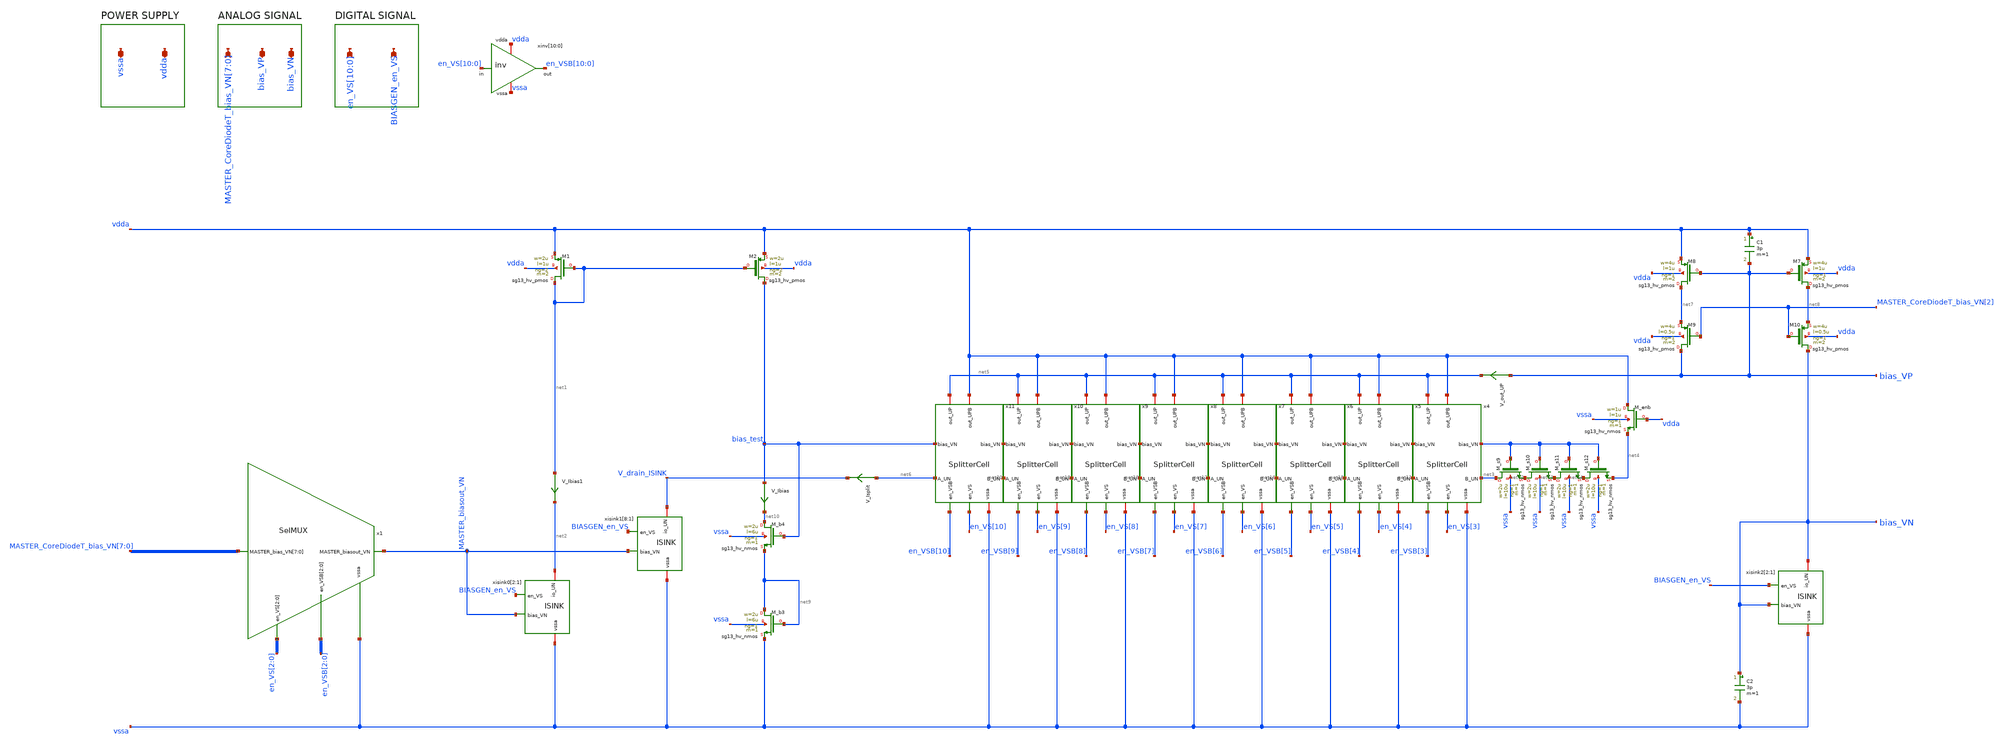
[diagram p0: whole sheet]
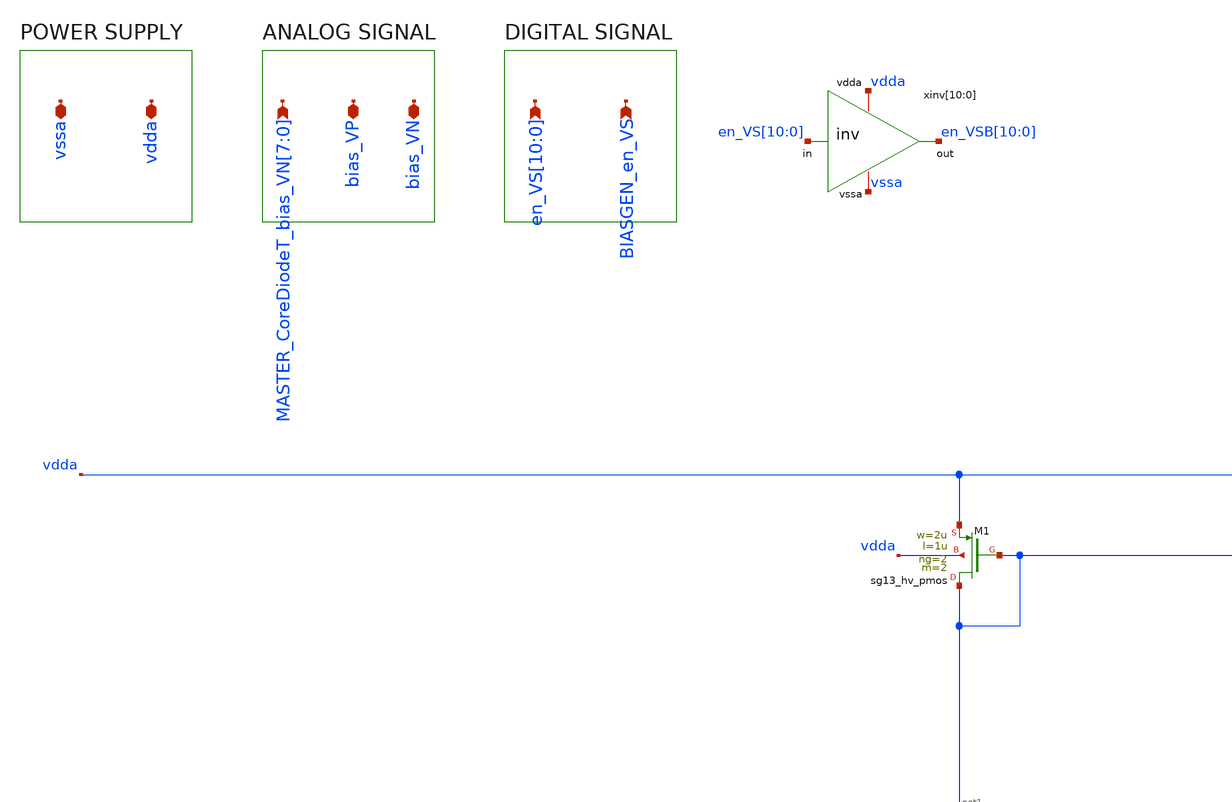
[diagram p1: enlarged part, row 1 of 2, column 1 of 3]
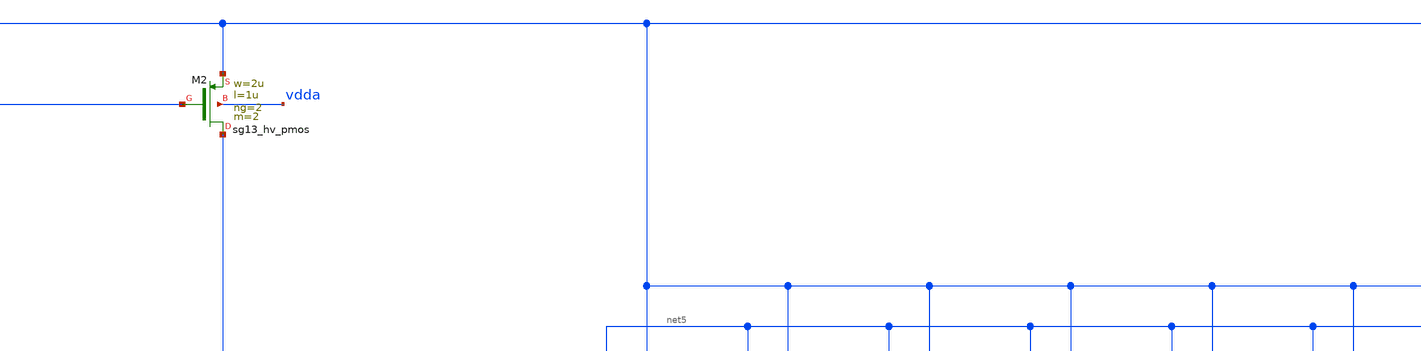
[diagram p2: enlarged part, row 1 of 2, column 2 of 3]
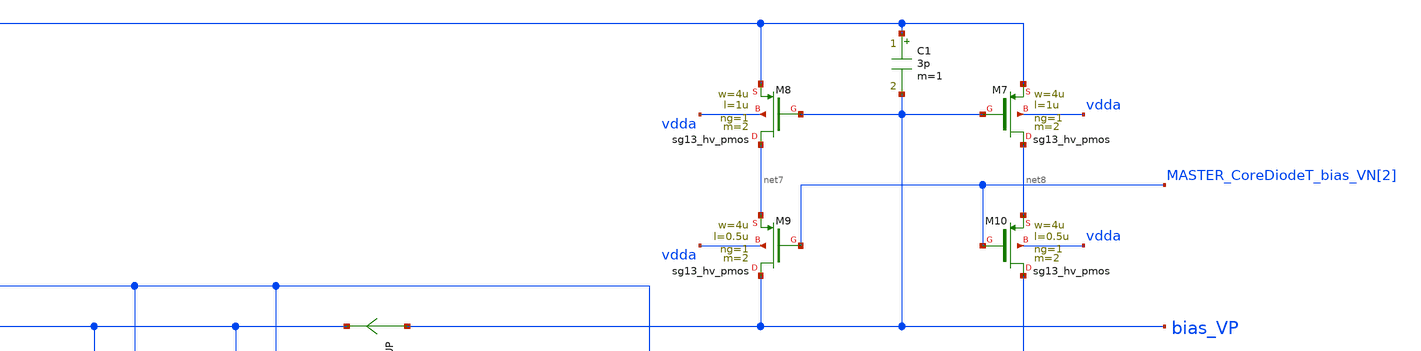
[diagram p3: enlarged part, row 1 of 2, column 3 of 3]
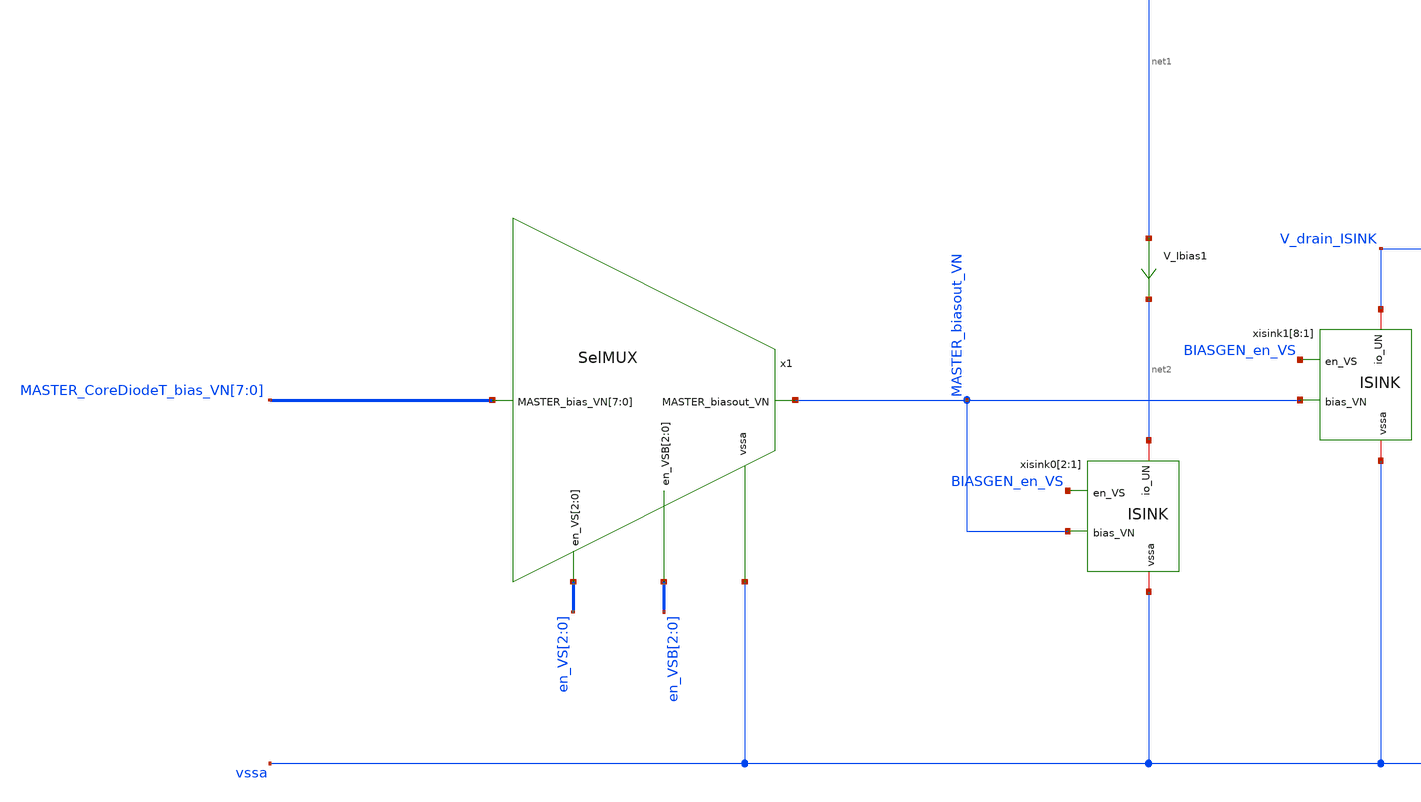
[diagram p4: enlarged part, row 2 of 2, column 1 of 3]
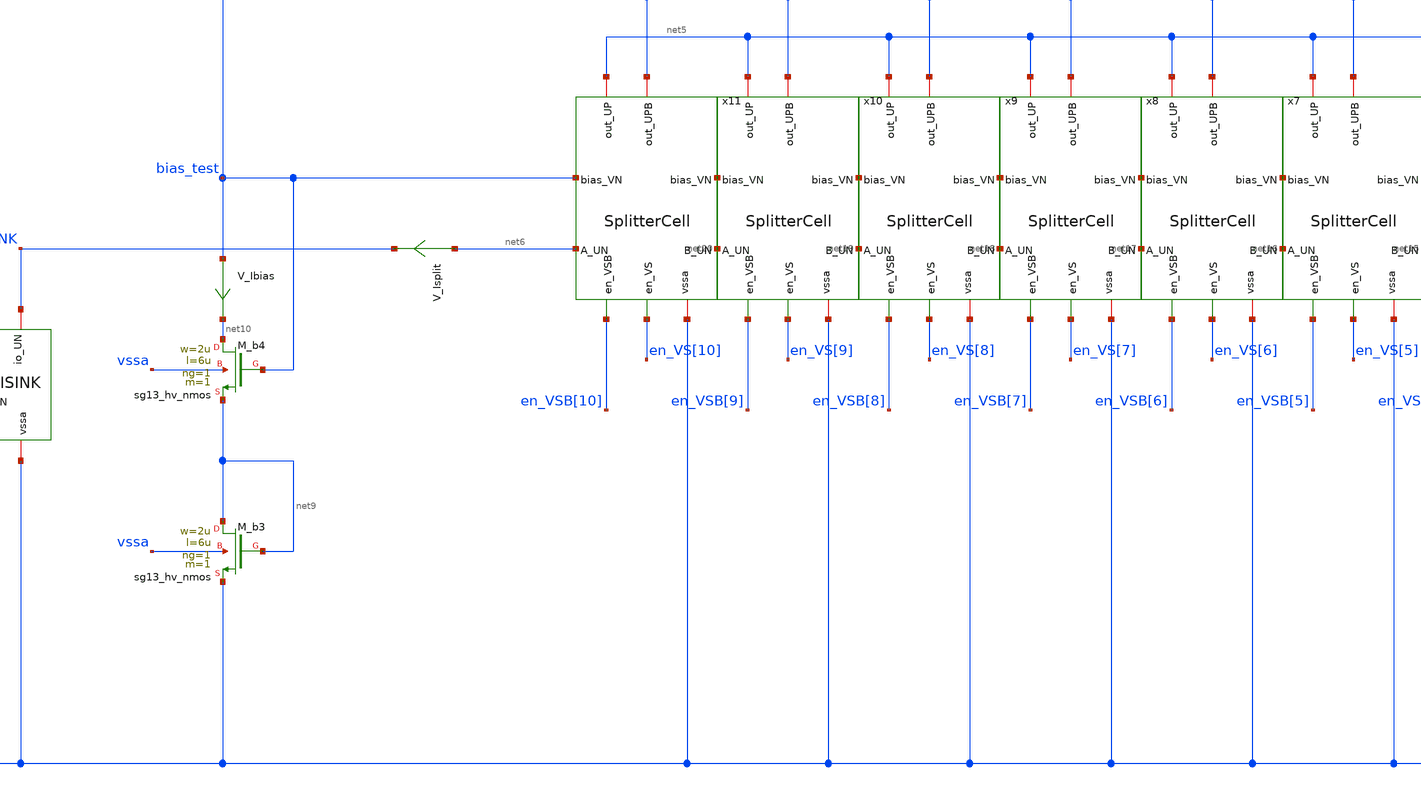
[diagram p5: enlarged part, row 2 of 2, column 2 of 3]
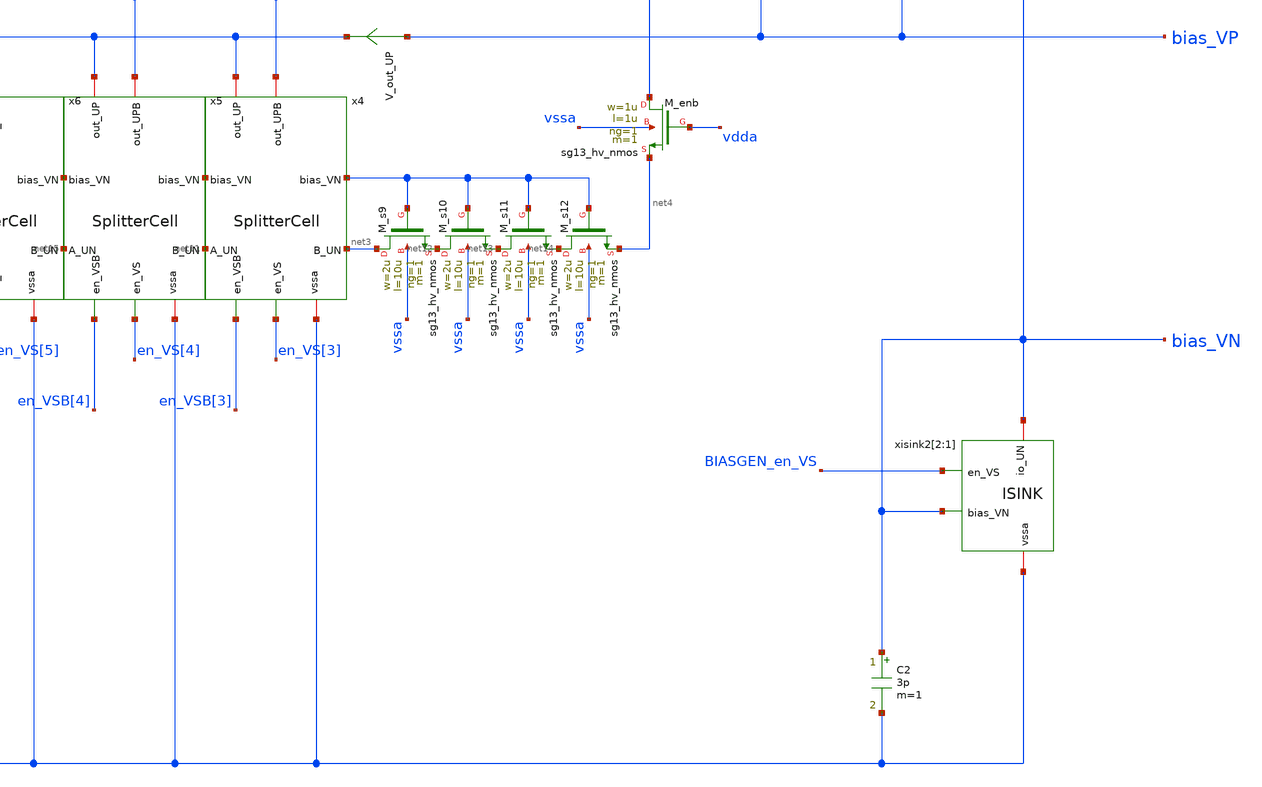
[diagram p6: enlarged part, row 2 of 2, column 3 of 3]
** sch_path: CoreFineDAC_N.sch
**.subckt CoreFineDAC_N
*+ MASTER_CoreDiodeT_bias_VN[7],MASTER_CoreDiodeT_bias_VN[6],MASTER_CoreDiodeT_bias_VN[5],MASTER_CoreDiodeT_bias_VN[4],MASTER_CoreDiodeT_bias_VN[3],MASTER_CoreDiodeT_bias_VN[2],MASTER_CoreDiodeT_bias_VN[1],MASTER_CoreDiodeT_bias_VN[0] en_VS[10],en_VS[9],en_VS[8],en_VS[7],en_VS[6],en_VS[5],en_VS[4],en_VS[3],en_VS[2],en_VS[1],en_VS[0]
*+ vssa vdda bias_VP bias_VN BIASGEN_en_VS
*.ipin
*+ MASTER_CoreDiodeT_bias_VN[7],MASTER_CoreDiodeT_bias_VN[6],MASTER_CoreDiodeT_bias_VN[5],MASTER_CoreDiodeT_bias_VN[4],MASTER_CoreDiodeT_bias_VN[3],MASTER_CoreDiodeT_bias_VN[2],MASTER_CoreDiodeT_bias_VN[1],MASTER_CoreDiodeT_bias_VN[0]
*.ipin
*+ en_VS[10],en_VS[9],en_VS[8],en_VS[7],en_VS[6],en_VS[5],en_VS[4],en_VS[3],en_VS[2],en_VS[1],en_VS[0]
*.iopin vssa
*.iopin vdda
*.iopin bias_VP
*.iopin bias_VN
*.ipin BIASGEN_en_VS
xinv[10] vdda en_VSB[10] en_VS[10] vssa inv
xinv[9] vdda en_VSB[9] en_VS[9] vssa inv
xinv[8] vdda en_VSB[8] en_VS[8] vssa inv
xinv[7] vdda en_VSB[7] en_VS[7] vssa inv
xinv[6] vdda en_VSB[6] en_VS[6] vssa inv
xinv[5] vdda en_VSB[5] en_VS[5] vssa inv
xinv[4] vdda en_VSB[4] en_VS[4] vssa inv
xinv[3] vdda en_VSB[3] en_VS[3] vssa inv
xinv[2] vdda en_VSB[2] en_VS[2] vssa inv
xinv[1] vdda en_VSB[1] en_VS[1] vssa inv
xinv[0] vdda en_VSB[0] en_VS[0] vssa inv
x1 MASTER_CoreDiodeT_bias_VN[7] MASTER_CoreDiodeT_bias_VN[6] MASTER_CoreDiodeT_bias_VN[5]
+ MASTER_CoreDiodeT_bias_VN[4] MASTER_CoreDiodeT_bias_VN[3] MASTER_CoreDiodeT_bias_VN[2] MASTER_CoreDiodeT_bias_VN[1]
+ MASTER_CoreDiodeT_bias_VN[0] vssa en_VS[2] en_VS[1] en_VS[0] en_VSB[2] en_VSB[1] en_VSB[0] MASTER_biasout_VN SelMUX
xisink0[2] MASTER_biasout_VN vssa BIASGEN_en_VS net2 ISINK
xisink0[1] MASTER_biasout_VN vssa BIASGEN_en_VS net2 ISINK
XM1 net1 net1 vdda vdda sg13_hv_pmos w=2u l=1u ng=2 m=2 mm_ok=1
XM2 bias_test net1 vdda vdda sg13_hv_pmos w=2u l=1u ng=2 m=2 mm_ok=1
x4 en_VS[3] net11 net3 en_VSB[3] bias_test vssa vdda net5 SplitterCell
XM_enb vdda vdda net4 vssa sg13_hv_nmos w=1u l=1u ng=1 m=1 mm_ok=1
XM_s9 net3 bias_test net12 vssa sg13_hv_nmos w=2u l=10u ng=1 m=1 mm_ok=1
XM_s10 net12 bias_test net13 vssa sg13_hv_nmos w=2u l=10u ng=1 m=1 mm_ok=1
XM_s11 net13 bias_test net14 vssa sg13_hv_nmos w=2u l=10u ng=1 m=1 mm_ok=1
XM_s12 net14 bias_test net4 vssa sg13_hv_nmos w=2u l=10u ng=1 m=1 mm_ok=1
V_out_UP bias_VP net5 0
.save i(v_out_up)
x5 en_VS[4] net15 net11 en_VSB[4] bias_test vssa vdda net5 SplitterCell
x6 en_VS[5] net16 net15 en_VSB[5] bias_test vssa vdda net5 SplitterCell
x7 en_VS[6] net17 net16 en_VSB[6] bias_test vssa vdda net5 SplitterCell
x8 en_VS[7] net18 net17 en_VSB[7] bias_test vssa vdda net5 SplitterCell
x9 en_VS[8] net19 net18 en_VSB[8] bias_test vssa vdda net5 SplitterCell
x10 en_VS[9] net20 net19 en_VSB[9] bias_test vssa vdda net5 SplitterCell
x11 en_VS[10] net6 net20 en_VSB[10] bias_test vssa vdda net5 SplitterCell
V_Isplit net6 V_drain_ISINK 0
.save i(v_isplit)
XM8 net7 bias_VP vdda vdda sg13_hv_pmos w=4u l=1u ng=1 m=2 mm_ok=1
XM7 net8 bias_VP vdda vdda sg13_hv_pmos w=4u l=1u ng=1 m=2 mm_ok=1
XM9 bias_VP MASTER_CoreDiodeT_bias_VN[2] net7 vdda sg13_hv_pmos w=4u l=0.5u ng=1 m=2 mm_ok=1
XM10 bias_VN MASTER_CoreDiodeT_bias_VN[2] net8 vdda sg13_hv_pmos w=4u l=0.5u ng=1 m=2 mm_ok=1
C1 vdda bias_VP 3p m=1
xisink2[2] bias_VN vssa BIASGEN_en_VS bias_VN ISINK
xisink2[1] bias_VN vssa BIASGEN_en_VS bias_VN ISINK
C2 bias_VN vssa 3p m=1
V_Ibias bias_test net10 0
.save i(v_ibias)
V_Ibias1 net1 net2 0
.save i(v_ibias1)
XM_b4 net10 bias_test net9 vssa sg13_hv_nmos w=2u l=6u ng=1 m=1 mm_ok=1
xisink1[8] MASTER_biasout_VN vssa BIASGEN_en_VS V_drain_ISINK ISINK
xisink1[7] MASTER_biasout_VN vssa BIASGEN_en_VS V_drain_ISINK ISINK
xisink1[6] MASTER_biasout_VN vssa BIASGEN_en_VS V_drain_ISINK ISINK
xisink1[5] MASTER_biasout_VN vssa BIASGEN_en_VS V_drain_ISINK ISINK
xisink1[4] MASTER_biasout_VN vssa BIASGEN_en_VS V_drain_ISINK ISINK
xisink1[3] MASTER_biasout_VN vssa BIASGEN_en_VS V_drain_ISINK ISINK
xisink1[2] MASTER_biasout_VN vssa BIASGEN_en_VS V_drain_ISINK ISINK
xisink1[1] MASTER_biasout_VN vssa BIASGEN_en_VS V_drain_ISINK ISINK
XM_b3 net9 net9 vssa vssa sg13_hv_nmos w=2u l=6u ng=1 m=1 mm_ok=1
**.ends
.end
